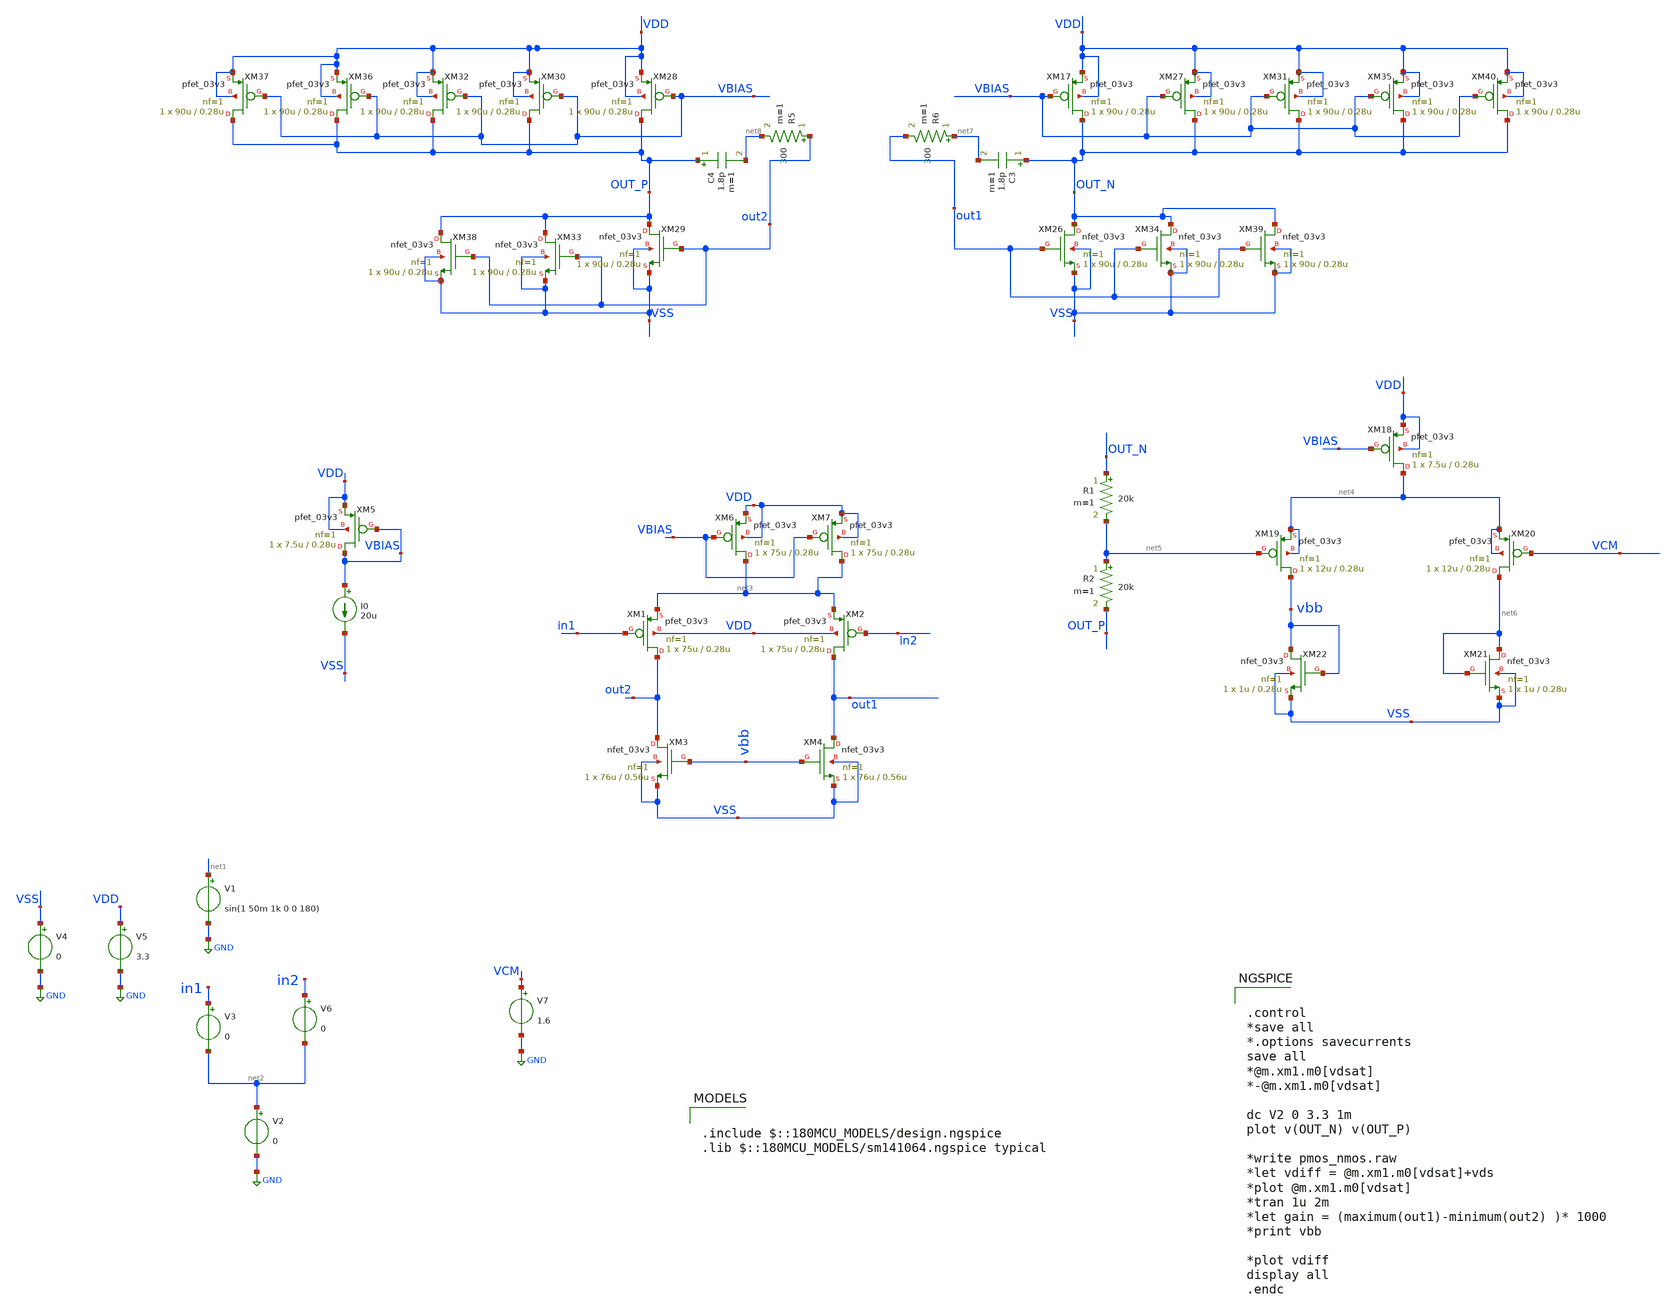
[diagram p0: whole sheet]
** sch_path: SCOP_INPUT_AND_MUX_PAKISTAN_03/Xschem/Folded_single/OTA_two_stage.sch
**.subckt OTA_two_stage
V1 net1 GND sin(1 50m 1k 0 0 180)
V3 in1 net2 0
V4 VSS GND 0
V5 VDD GND 3.3
V6 in2 net2 0
V7 VCM GND 1.6
XM1 out2 in1 net3 VDD pfet_03v3 L=0.28u W=75u nf=1 ad='int((nf+1)/2) * W/nf * 0.18u' as='int((nf+2)/2) * W/nf * 0.18u'
+ pd='2*int((nf+1)/2) * (W/nf + 0.18u)' ps='2*int((nf+2)/2) * (W/nf + 0.18u)' nrd='0.18u / W' nrs='0.18u / W'
+ sa=0 sb=0 sd=0 m=1
XM2 out1 in2 net3 VDD pfet_03v3 L=0.28u W=75u nf=1 ad='int((nf+1)/2) * W/nf * 0.18u' as='int((nf+2)/2) * W/nf * 0.18u'
+ pd='2*int((nf+1)/2) * (W/nf + 0.18u)' ps='2*int((nf+2)/2) * (W/nf + 0.18u)' nrd='0.18u / W' nrs='0.18u / W'
+ sa=0 sb=0 sd=0 m=1
XM3 out2 vbb VSS VSS nfet_03v3 L=0.56u W=76u nf=1 ad='int((nf+1)/2) * W/nf * 0.18u' as='int((nf+2)/2) * W/nf * 0.18u'
+ pd='2*int((nf+1)/2) * (W/nf + 0.18u)' ps='2*int((nf+2)/2) * (W/nf + 0.18u)' nrd='0.18u / W' nrs='0.18u / W'
+ sa=0 sb=0 sd=0 m=1
XM4 out1 vbb VSS VSS nfet_03v3 L=0.56u W=76u nf=1 ad='int((nf+1)/2) * W/nf * 0.18u' as='int((nf+2)/2) * W/nf * 0.18u'
+ pd='2*int((nf+1)/2) * (W/nf + 0.18u)' ps='2*int((nf+2)/2) * (W/nf + 0.18u)' nrd='0.18u / W' nrs='0.18u / W'
+ sa=0 sb=0 sd=0 m=1
XM5 VBIAS VBIAS VDD VDD pfet_03v3 L=0.28u W=7.5u nf=1 ad='int((nf+1)/2) * W/nf * 0.18u' as='int((nf+2)/2) * W/nf * 0.18u'
+ pd='2*int((nf+1)/2) * (W/nf + 0.18u)' ps='2*int((nf+2)/2) * (W/nf + 0.18u)' nrd='0.18u / W' nrs='0.18u / W'
+ sa=0 sb=0 sd=0 m=1
I0 VBIAS VSS 20u
XM18 net4 VBIAS VDD VDD pfet_03v3 L=0.28u W=7.5u nf=1 ad='int((nf+1)/2) * W/nf * 0.18u' as='int((nf+2)/2) * W/nf * 0.18u'
+ pd='2*int((nf+1)/2) * (W/nf + 0.18u)' ps='2*int((nf+2)/2) * (W/nf + 0.18u)' nrd='0.18u / W' nrs='0.18u / W'
+ sa=0 sb=0 sd=0 m=1
XM19 vbb net5 net4 net4 pfet_03v3 L=0.28u W=12u nf=1 ad='int((nf+1)/2) * W/nf * 0.18u' as='int((nf+2)/2) * W/nf * 0.18u'
+ pd='2*int((nf+1)/2) * (W/nf + 0.18u)' ps='2*int((nf+2)/2) * (W/nf + 0.18u)' nrd='0.18u / W' nrs='0.18u / W'
+ sa=0 sb=0 sd=0 m=1
XM20 net6 VCM net4 net4 pfet_03v3 L=0.28u W=12u nf=1 ad='int((nf+1)/2) * W/nf * 0.18u' as='int((nf+2)/2) * W/nf * 0.18u'
+ pd='2*int((nf+1)/2) * (W/nf + 0.18u)' ps='2*int((nf+2)/2) * (W/nf + 0.18u)' nrd='0.18u / W' nrs='0.18u / W'
+ sa=0 sb=0 sd=0 m=1
XM21 net6 net6 VSS VSS nfet_03v3 L=0.28u W=1u nf=1 ad='int((nf+1)/2) * W/nf * 0.18u' as='int((nf+2)/2) * W/nf * 0.18u'
+ pd='2*int((nf+1)/2) * (W/nf + 0.18u)' ps='2*int((nf+2)/2) * (W/nf + 0.18u)' nrd='0.18u / W' nrs='0.18u / W'
+ sa=0 sb=0 sd=0 m=1
XM22 vbb vbb VSS VSS nfet_03v3 L=0.28u W=1u nf=1 ad='int((nf+1)/2) * W/nf * 0.18u' as='int((nf+2)/2) * W/nf * 0.18u'
+ pd='2*int((nf+1)/2) * (W/nf + 0.18u)' ps='2*int((nf+2)/2) * (W/nf + 0.18u)' nrd='0.18u / W' nrs='0.18u / W'
+ sa=0 sb=0 sd=0 m=1
R1 OUT_N net5 20k m=1
R2 net5 OUT_P 20k m=1
XM6 net3 VBIAS VDD VDD pfet_03v3 L=0.28u W=75u nf=1 ad='int((nf+1)/2) * W/nf * 0.18u' as='int((nf+2)/2) * W/nf * 0.18u'
+ pd='2*int((nf+1)/2) * (W/nf + 0.18u)' ps='2*int((nf+2)/2) * (W/nf + 0.18u)' nrd='0.18u / W' nrs='0.18u / W'
+ sa=0 sb=0 sd=0 m=1
XM7 net3 VBIAS VDD VDD pfet_03v3 L=0.28u W=75u nf=1 ad='int((nf+1)/2) * W/nf * 0.18u' as='int((nf+2)/2) * W/nf * 0.18u'
+ pd='2*int((nf+1)/2) * (W/nf + 0.18u)' ps='2*int((nf+2)/2) * (W/nf + 0.18u)' nrd='0.18u / W' nrs='0.18u / W'
+ sa=0 sb=0 sd=0 m=1
V2 net2 GND 0
XM17 OUT_N VBIAS VDD VDD pfet_03v3 L=0.28u W=90u nf=1 ad='int((nf+1)/2) * W/nf * 0.18u' as='int((nf+2)/2) * W/nf * 0.18u'
+ pd='2*int((nf+1)/2) * (W/nf + 0.18u)' ps='2*int((nf+2)/2) * (W/nf + 0.18u)' nrd='0.18u / W' nrs='0.18u / W'
+ sa=0 sb=0 sd=0 m=1
XM26 OUT_N out1 VSS VSS nfet_03v3 L=0.28u W=90u nf=1 ad='int((nf+1)/2) * W/nf * 0.18u' as='int((nf+2)/2) * W/nf * 0.18u'
+ pd='2*int((nf+1)/2) * (W/nf + 0.18u)' ps='2*int((nf+2)/2) * (W/nf + 0.18u)' nrd='0.18u / W' nrs='0.18u / W'
+ sa=0 sb=0 sd=0 m=1
C3 OUT_N net7 1.8p m=1
XM27 OUT_N VBIAS VDD VDD pfet_03v3 L=0.28u W=90u nf=1 ad='int((nf+1)/2) * W/nf * 0.18u' as='int((nf+2)/2) * W/nf * 0.18u'
+ pd='2*int((nf+1)/2) * (W/nf + 0.18u)' ps='2*int((nf+2)/2) * (W/nf + 0.18u)' nrd='0.18u / W' nrs='0.18u / W'
+ sa=0 sb=0 sd=0 m=1
XM28 OUT_P VBIAS VDD VDD pfet_03v3 L=0.28u W=90u nf=1 ad='int((nf+1)/2) * W/nf * 0.18u' as='int((nf+2)/2) * W/nf * 0.18u'
+ pd='2*int((nf+1)/2) * (W/nf + 0.18u)' ps='2*int((nf+2)/2) * (W/nf + 0.18u)' nrd='0.18u / W' nrs='0.18u / W'
+ sa=0 sb=0 sd=0 m=1
XM29 OUT_P out2 VSS VSS nfet_03v3 L=0.28u W=90u nf=1 ad='int((nf+1)/2) * W/nf * 0.18u' as='int((nf+2)/2) * W/nf * 0.18u'
+ pd='2*int((nf+1)/2) * (W/nf + 0.18u)' ps='2*int((nf+2)/2) * (W/nf + 0.18u)' nrd='0.18u / W' nrs='0.18u / W'
+ sa=0 sb=0 sd=0 m=1
C4 OUT_P net8 1.8p m=1
XM30 OUT_P VBIAS VDD VDD pfet_03v3 L=0.28u W=90u nf=1 ad='int((nf+1)/2) * W/nf * 0.18u' as='int((nf+2)/2) * W/nf * 0.18u'
+ pd='2*int((nf+1)/2) * (W/nf + 0.18u)' ps='2*int((nf+2)/2) * (W/nf + 0.18u)' nrd='0.18u / W' nrs='0.18u / W'
+ sa=0 sb=0 sd=0 m=1
R5 out2 net8 300 m=1
R6 net7 out1 300 m=1
XM31 OUT_N VBIAS VDD VDD pfet_03v3 L=0.28u W=90u nf=1 ad='int((nf+1)/2) * W/nf * 0.18u' as='int((nf+2)/2) * W/nf * 0.18u'
+ pd='2*int((nf+1)/2) * (W/nf + 0.18u)' ps='2*int((nf+2)/2) * (W/nf + 0.18u)' nrd='0.18u / W' nrs='0.18u / W'
+ sa=0 sb=0 sd=0 m=1
XM32 OUT_P VBIAS VDD VDD pfet_03v3 L=0.28u W=90u nf=1 ad='int((nf+1)/2) * W/nf * 0.18u' as='int((nf+2)/2) * W/nf * 0.18u'
+ pd='2*int((nf+1)/2) * (W/nf + 0.18u)' ps='2*int((nf+2)/2) * (W/nf + 0.18u)' nrd='0.18u / W' nrs='0.18u / W'
+ sa=0 sb=0 sd=0 m=1
XM33 OUT_P out2 VSS VSS nfet_03v3 L=0.28u W=90u nf=1 ad='int((nf+1)/2) * W/nf * 0.18u' as='int((nf+2)/2) * W/nf * 0.18u'
+ pd='2*int((nf+1)/2) * (W/nf + 0.18u)' ps='2*int((nf+2)/2) * (W/nf + 0.18u)' nrd='0.18u / W' nrs='0.18u / W'
+ sa=0 sb=0 sd=0 m=1
XM34 OUT_N out1 VSS VSS nfet_03v3 L=0.28u W=90u nf=1 ad='int((nf+1)/2) * W/nf * 0.18u' as='int((nf+2)/2) * W/nf * 0.18u'
+ pd='2*int((nf+1)/2) * (W/nf + 0.18u)' ps='2*int((nf+2)/2) * (W/nf + 0.18u)' nrd='0.18u / W' nrs='0.18u / W'
+ sa=0 sb=0 sd=0 m=1
XM35 OUT_N VBIAS VDD VDD pfet_03v3 L=0.28u W=90u nf=1 ad='int((nf+1)/2) * W/nf * 0.18u' as='int((nf+2)/2) * W/nf * 0.18u'
+ pd='2*int((nf+1)/2) * (W/nf + 0.18u)' ps='2*int((nf+2)/2) * (W/nf + 0.18u)' nrd='0.18u / W' nrs='0.18u / W'
+ sa=0 sb=0 sd=0 m=1
XM36 OUT_P VBIAS VDD VDD pfet_03v3 L=0.28u W=90u nf=1 ad='int((nf+1)/2) * W/nf * 0.18u' as='int((nf+2)/2) * W/nf * 0.18u'
+ pd='2*int((nf+1)/2) * (W/nf + 0.18u)' ps='2*int((nf+2)/2) * (W/nf + 0.18u)' nrd='0.18u / W' nrs='0.18u / W'
+ sa=0 sb=0 sd=0 m=1
XM37 OUT_P VBIAS VDD VDD pfet_03v3 L=0.28u W=90u nf=1 ad='int((nf+1)/2) * W/nf * 0.18u' as='int((nf+2)/2) * W/nf * 0.18u'
+ pd='2*int((nf+1)/2) * (W/nf + 0.18u)' ps='2*int((nf+2)/2) * (W/nf + 0.18u)' nrd='0.18u / W' nrs='0.18u / W'
+ sa=0 sb=0 sd=0 m=1
XM38 OUT_P out2 VSS VSS nfet_03v3 L=0.28u W=90u nf=1 ad='int((nf+1)/2) * W/nf * 0.18u' as='int((nf+2)/2) * W/nf * 0.18u'
+ pd='2*int((nf+1)/2) * (W/nf + 0.18u)' ps='2*int((nf+2)/2) * (W/nf + 0.18u)' nrd='0.18u / W' nrs='0.18u / W'
+ sa=0 sb=0 sd=0 m=1
XM39 OUT_N out1 VSS VSS nfet_03v3 L=0.28u W=90u nf=1 ad='int((nf+1)/2) * W/nf * 0.18u' as='int((nf+2)/2) * W/nf * 0.18u'
+ pd='2*int((nf+1)/2) * (W/nf + 0.18u)' ps='2*int((nf+2)/2) * (W/nf + 0.18u)' nrd='0.18u / W' nrs='0.18u / W'
+ sa=0 sb=0 sd=0 m=1
XM40 OUT_N VBIAS VDD VDD pfet_03v3 L=0.28u W=90u nf=1 ad='int((nf+1)/2) * W/nf * 0.18u' as='int((nf+2)/2) * W/nf * 0.18u'
+ pd='2*int((nf+1)/2) * (W/nf + 0.18u)' ps='2*int((nf+2)/2) * (W/nf + 0.18u)' nrd='0.18u / W' nrs='0.18u / W'
+ sa=0 sb=0 sd=0 m=1
**** begin user architecture code

.include $::180MCU_MODELS/design.ngspice
.lib $::180MCU_MODELS/sm141064.ngspice typical



.control
*save all
*.options savecurrents
save all
*@m.xm1.m0[vdsat]
*-@m.xm1.m0[vdsat]

dc V2 0 3.3 1m
plot v(OUT_N) v(OUT_P)

*write pmos_nmos.raw
*let vdiff = @m.xm1.m0[vdsat]+vds
*plot @m.xm1.m0[vdsat]
*tran 1u 2m
*let gain = (maximum(out1)-minimum(out2) )* 1000
*print vbb

*plot vdiff
display all
.endc


**** end user architecture code
**.ends
.GLOBAL GND
.end
